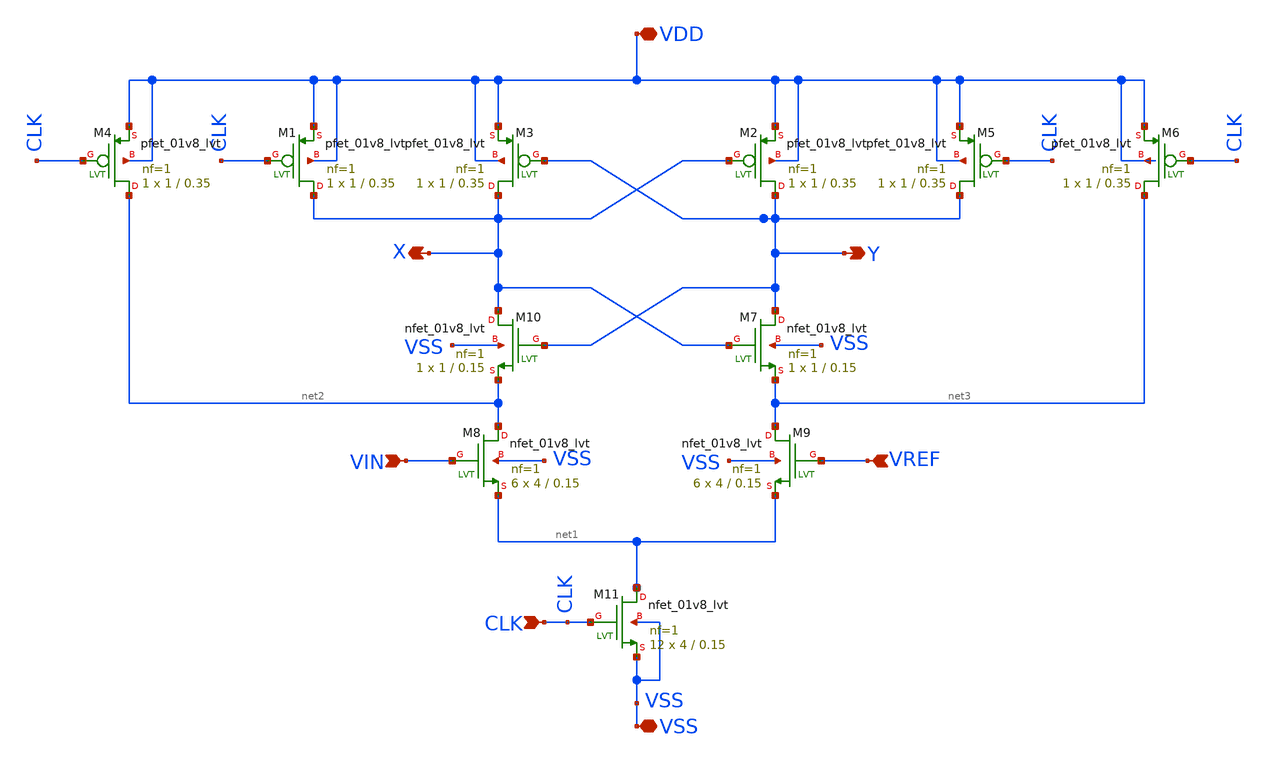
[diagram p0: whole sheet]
** sch_path: strongARM/strongARM_v2_sym.sch
**.subckt strongARM_v2_sym VDD VIN VREF Y X VSS CLK
*.iopin VDD
*.ipin VIN
*.ipin VREF
*.opin Y
*.opin X
*.iopin VSS
*.ipin CLK
XM4 net2 CLK VDD VDD sky130_fd_pr__pfet_01v8_lvt L=0.35 W=1 nf=1 ad='int((nf+1)/2) * W/nf * 0.29' as='int((nf+2)/2) * W/nf * 0.29'
+ pd='2*int((nf+1)/2) * (W/nf + 0.29)' ps='2*int((nf+2)/2) * (W/nf + 0.29)' nrd='0.29 / W' nrs='0.29 / W'
+ sa=0 sb=0 sd=0 mult=1 m=1
XM1 X CLK VDD VDD sky130_fd_pr__pfet_01v8_lvt L=0.35 W=1 nf=1 ad='int((nf+1)/2) * W/nf * 0.29' as='int((nf+2)/2) * W/nf * 0.29'
+ pd='2*int((nf+1)/2) * (W/nf + 0.29)' ps='2*int((nf+2)/2) * (W/nf + 0.29)' nrd='0.29 / W' nrs='0.29 / W'
+ sa=0 sb=0 sd=0 mult=1 m=1
XM2 Y X VDD VDD sky130_fd_pr__pfet_01v8_lvt L=0.35 W=1 nf=1 ad='int((nf+1)/2) * W/nf * 0.29' as='int((nf+2)/2) * W/nf * 0.29'
+ pd='2*int((nf+1)/2) * (W/nf + 0.29)' ps='2*int((nf+2)/2) * (W/nf + 0.29)' nrd='0.29 / W' nrs='0.29 / W'
+ sa=0 sb=0 sd=0 mult=1 m=1
XM3 X Y VDD VDD sky130_fd_pr__pfet_01v8_lvt L=0.35 W=1 nf=1 ad='int((nf+1)/2) * W/nf * 0.29' as='int((nf+2)/2) * W/nf * 0.29'
+ pd='2*int((nf+1)/2) * (W/nf + 0.29)' ps='2*int((nf+2)/2) * (W/nf + 0.29)' nrd='0.29 / W' nrs='0.29 / W'
+ sa=0 sb=0 sd=0 mult=1 m=1
XM5 Y CLK VDD VDD sky130_fd_pr__pfet_01v8_lvt L=0.35 W=1 nf=1 ad='int((nf+1)/2) * W/nf * 0.29' as='int((nf+2)/2) * W/nf * 0.29'
+ pd='2*int((nf+1)/2) * (W/nf + 0.29)' ps='2*int((nf+2)/2) * (W/nf + 0.29)' nrd='0.29 / W' nrs='0.29 / W'
+ sa=0 sb=0 sd=0 mult=1 m=1
XM6 net3 CLK VDD VDD sky130_fd_pr__pfet_01v8_lvt L=0.35 W=1 nf=1 ad='int((nf+1)/2) * W/nf * 0.29' as='int((nf+2)/2) * W/nf * 0.29'
+ pd='2*int((nf+1)/2) * (W/nf + 0.29)' ps='2*int((nf+2)/2) * (W/nf + 0.29)' nrd='0.29 / W' nrs='0.29 / W'
+ sa=0 sb=0 sd=0 mult=1 m=1
XM10 X Y net2 VSS sky130_fd_pr__nfet_01v8_lvt L=0.15 W=1 nf=1 ad='int((nf+1)/2) * W/nf * 0.29' as='int((nf+2)/2) * W/nf * 0.29'
+ pd='2*int((nf+1)/2) * (W/nf + 0.29)' ps='2*int((nf+2)/2) * (W/nf + 0.29)' nrd='0.29 / W' nrs='0.29 / W'
+ sa=0 sb=0 sd=0 mult=1 m=1
XM7 Y X net3 VSS sky130_fd_pr__nfet_01v8_lvt L=0.15 W=1 nf=1 ad='int((nf+1)/2) * W/nf * 0.29' as='int((nf+2)/2) * W/nf * 0.29'
+ pd='2*int((nf+1)/2) * (W/nf + 0.29)' ps='2*int((nf+2)/2) * (W/nf + 0.29)' nrd='0.29 / W' nrs='0.29 / W'
+ sa=0 sb=0 sd=0 mult=1 m=1
XM8 net2 VIN net1 VSS sky130_fd_pr__nfet_01v8_lvt L=0.15 W=4 nf=1 ad='int((nf+1)/2) * W/nf * 0.29' as='int((nf+2)/2) * W/nf * 0.29'
+ pd='2*int((nf+1)/2) * (W/nf + 0.29)' ps='2*int((nf+2)/2) * (W/nf + 0.29)' nrd='0.29 / W' nrs='0.29 / W'
+ sa=0 sb=0 sd=0 mult=6 m=6
XM9 net3 VREF net1 VSS sky130_fd_pr__nfet_01v8_lvt L=0.15 W=4 nf=1 ad='int((nf+1)/2) * W/nf * 0.29' as='int((nf+2)/2) * W/nf * 0.29'
+ pd='2*int((nf+1)/2) * (W/nf + 0.29)' ps='2*int((nf+2)/2) * (W/nf + 0.29)' nrd='0.29 / W' nrs='0.29 / W'
+ sa=0 sb=0 sd=0 mult=6 m=6
XM11 net1 CLK VSS VSS sky130_fd_pr__nfet_01v8_lvt L=0.15 W=4 nf=1 ad='int((nf+1)/2) * W/nf * 0.29' as='int((nf+2)/2) * W/nf * 0.29'
+ pd='2*int((nf+1)/2) * (W/nf + 0.29)' ps='2*int((nf+2)/2) * (W/nf + 0.29)' nrd='0.29 / W' nrs='0.29 / W'
+ sa=0 sb=0 sd=0 mult=12 m=12
**.ends
.end
